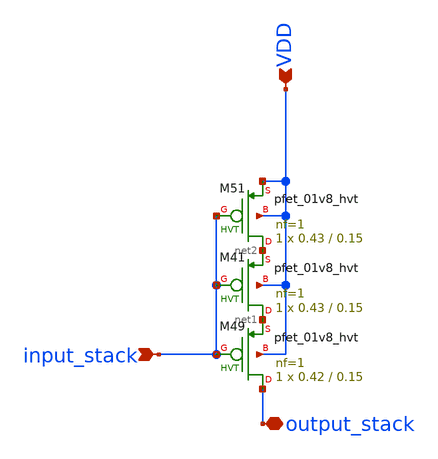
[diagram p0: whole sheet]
** sch_path: hgu/xschem/hgu_pfet_hvt_stack_in_delay.sch
**.subckt hgu_pfet_hvt_stack_in_delay VDD input_stack output_stack
*.ipin VDD
*.ipin input_stack
*.iopin output_stack
XM49 output_stack input_stack net1 VDD sky130_fd_pr__pfet_01v8_hvt L=0.15 W=0.42 nf=1 ad='int((nf+1)/2) * W/nf * 0.29'
+ as='int((nf+2)/2) * W/nf * 0.29' pd='2*int((nf+1)/2) * (W/nf + 0.29)' ps='2*int((nf+2)/2) * (W/nf + 0.29)'
+ nrd='0.29 / W' nrs='0.29 / W' sa=0 sb=0 sd=0 mult=1 m=1
XM41 net1 input_stack net2 VDD sky130_fd_pr__pfet_01v8_hvt L=0.15 W=0.43 nf=1 ad='int((nf+1)/2) * W/nf * 0.29'
+ as='int((nf+2)/2) * W/nf * 0.29' pd='2*int((nf+1)/2) * (W/nf + 0.29)' ps='2*int((nf+2)/2) * (W/nf + 0.29)'
+ nrd='0.29 / W' nrs='0.29 / W' sa=0 sb=0 sd=0 mult=1 m=1
XM51 net2 input_stack VDD VDD sky130_fd_pr__pfet_01v8_hvt L=0.15 W=0.43 nf=1 ad='int((nf+1)/2) * W/nf * 0.29'
+ as='int((nf+2)/2) * W/nf * 0.29' pd='2*int((nf+1)/2) * (W/nf + 0.29)' ps='2*int((nf+2)/2) * (W/nf + 0.29)'
+ nrd='0.29 / W' nrs='0.29 / W' sa=0 sb=0 sd=0 mult=1 m=1
**.ends
.end
